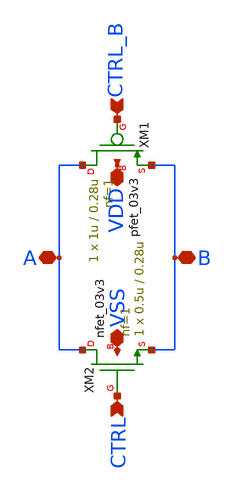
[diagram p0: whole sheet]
** sch_path: sar_logic/sar_designs/tg.sch
**.subckt tg VDD VSS A B CTRL_B CTRL
*.iopin VDD
*.iopin VSS
*.iopin A
*.iopin B
*.ipin CTRL_B
*.ipin CTRL
XM1 A CTRL_B B VDD pfet_03v3 L=0.28u W=1u nf=1 ad='int((nf+1)/2) * W/nf * 0.18u' as='int((nf+2)/2) * W/nf * 0.18u'
+ pd='2*int((nf+1)/2) * (W/nf + 0.18u)' ps='2*int((nf+2)/2) * (W/nf + 0.18u)' nrd='0.18u / W' nrs='0.18u / W'
+ sa=0 sb=0 sd=0 m=1
XM2 A CTRL B VSS nfet_03v3 L=0.28u W=0.5u nf=1 ad='int((nf+1)/2) * W/nf * 0.18u' as='int((nf+2)/2) * W/nf * 0.18u'
+ pd='2*int((nf+1)/2) * (W/nf + 0.18u)' ps='2*int((nf+2)/2) * (W/nf + 0.18u)' nrd='0.18u / W' nrs='0.18u / W'
+ sa=0 sb=0 sd=0 m=1
**.ends
.end
